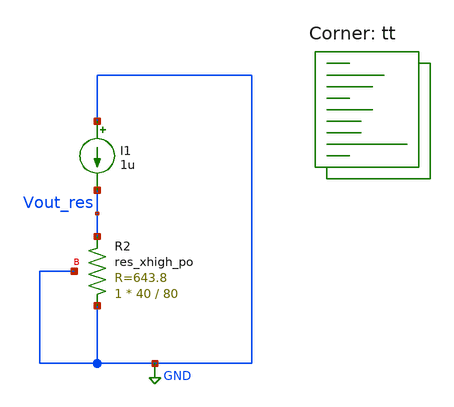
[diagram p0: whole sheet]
** sch_path: xschem/misc/testing/res_1p23k.sch
**.subckt res_1p23k
I1 GND Vout_res 1u
XR2 GND Vout_res GND sky130_fd_pr__res_xhigh_po W=40 L=80 mult=1 m=1
**** begin user architecture code
.lib $::SKYWATER_MODELS/sky130.lib.spice tt


.param temp=27

.dc temp -40 125 1


.save all
.control
run
plot Vout_res
plot deriv(Vout_res)
.endc



**** end user architecture code
**.ends
.GLOBAL GND
.end
